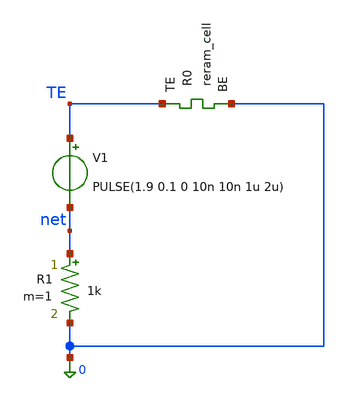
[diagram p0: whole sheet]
** sch_path: memristor_models/sky130_original/1R_well.sch
**.subckt 1R_well
V1 TE net PULSE(1.9 0.1 0 10n 10n 1u 2u)
XR0 TE 0 sky130_fd_pr_reram__reram_cell Tfilament_0=3.3e-9
R1 net 0 1k m=1
**** begin user architecture code

** opencircuitdesign pdks install
.inc /home/alex/Desktop/EDA/SNN_IPN/memristor_models/wellposed/rram_v0.spice



.option savecurrents
.tran 100n 1000u
.control
	save all
	run
	write 1R.raw
.endc



**** end user architecture code
**.ends
.end
